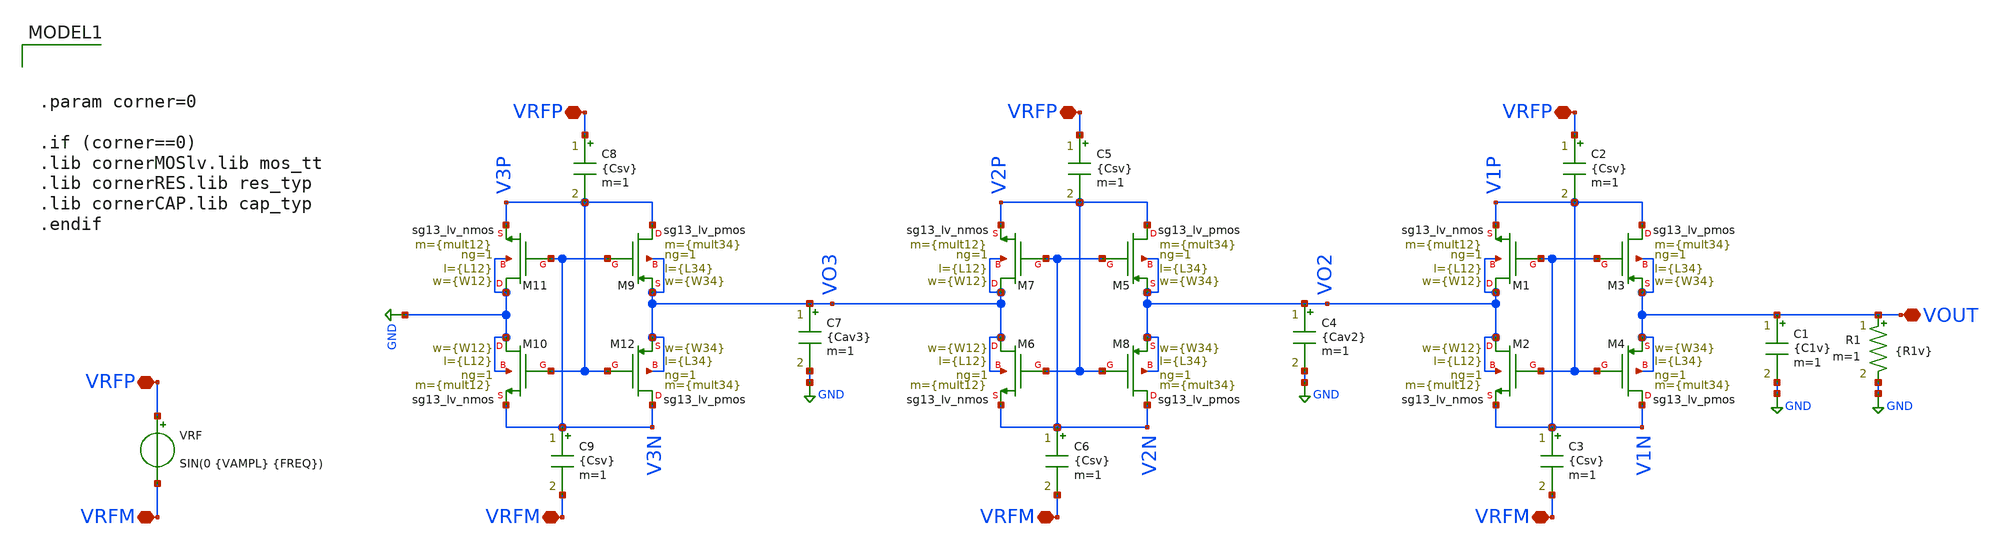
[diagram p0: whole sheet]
** sch_path: Esquematicos_Xschem/Memoria_CCDD_TRAN_MULT3.sch
**.subckt Memoria_CCDD_TRAN_MULT3 VRFP VRFM VOUT VRFP VRFM VRFP VRFM VRFP VRFM
*.iopin VRFP
*.iopin VRFM
*.iopin VOUT
*.iopin VRFP
*.iopin VRFM
*.iopin VRFP
*.iopin VRFM
*.iopin VRFP
*.iopin VRFM
XM3 V1P V1N VOUT VOUT sg13_lv_pmos w={W34} l={L34} ng=1 m={mult34} mm_ok=1
XM2 VO2 V1P V1N VO2 sg13_lv_nmos w={W12} l={L12} ng=1 m={mult12} mm_ok=1
XM1 VO2 V1N V1P VO2 sg13_lv_nmos w={W12} l={L12} ng=1 m={mult12} mm_ok=1
XM4 V1N V1P VOUT VOUT sg13_lv_pmos w={W34} l={L34} ng=1 m={mult34} mm_ok=1
R1 VOUT GND {R1v} m=1
C1 VOUT GND {C1v} m=1
VRF VRFP VRFM SIN(0 {VAMPL} {FREQ})
.save i(vrf)
C2 VRFP V1P {Csv} m=1
C3 V1N VRFM {Csv} m=1
XM5 V2P V2N VO2 VO2 sg13_lv_pmos w={W34} l={L34} ng=1 m={mult34} mm_ok=1
XM6 VO3 V2P V2N VO3 sg13_lv_nmos w={W12} l={L12} ng=1 m={mult12} mm_ok=1
XM7 VO3 V2N V2P VO3 sg13_lv_nmos w={W12} l={L12} ng=1 m={mult12} mm_ok=1
XM8 V2N V2P VO2 VO2 sg13_lv_pmos w={W34} l={L34} ng=1 m={mult34} mm_ok=1
C4 VO2 GND {Cav2} m=1
C5 VRFP V2P {Csv} m=1
C6 V2N VRFM {Csv} m=1
XM9 V3P V3N VO3 VO3 sg13_lv_pmos w={W34} l={L34} ng=1 m={mult34} mm_ok=1
XM10 GND V3P V3N GND sg13_lv_nmos w={W12} l={L12} ng=1 m={mult12} mm_ok=1
XM11 GND V3N V3P GND sg13_lv_nmos w={W12} l={L12} ng=1 m={mult12} mm_ok=1
XM12 V3N V3P VO3 VO3 sg13_lv_pmos w={W34} l={L34} ng=1 m={mult34} mm_ok=1
C7 VO3 GND {Cav3} m=1
C8 VRFP V3P {Csv} m=1
C9 V3N VRFM {Csv} m=1
**** begin user architecture code



.option wnflag=1
.savecurrents

* =============================
* PARAMETROS DE SIMULACION
* =============================

**** Parametros PMOS M3 y M4
.param L34 = 0.2u
.param W34 = 1.78u
.param mult34 = 40

**** Parametros NMOS M1 y M2
.param L12 = 0.2u
.param W12 = 0.6u
.param mult12 = 40

* Parametros PMOS M1
*.param Lval1 = 0.13u
*.param Wval1 = 0.15u
*.param mult1 = 5

* Parametros NMOS M2
*.param Lval2 = 1u
*.param Wval2 = 0.15u
*.param mult2 = 1

* Parametros NMOS M3
*.param Lval3 = 1u
*.param Wval3 = 0.15u
*.param mult3 = 1

* Parametros PMOS M4
*.param Lval4 = 1u
*.param Wval4 = 0.15u
*.param mult4 = 1

**** Parametros de Carga
.param C1v = 1p
.ic V(VOUT) = 0
.param R1v = 5k

**** Parametros de Acople
.param Csv = 4p
.param Cav2 = 2*1p
.param Cav3 = 3*1p
*.param Cav4 = 4*1p
*.param Cav5 = 5*1p

**** Parametros Fuente Sinusoidal
.param VAMPL = 0.1      ; Amplitud (V)
.param VOFFS = 0         ; Valor medio (V)
.param FREQ  = 900MEG        ; Frecuencia (Hz)
.param PHASE = 0         ; Fase1 (grados)








.option wnflag=1
.savecurrents

* ==============================================
* BLOQUE DE CONTROL NGSPICE
* ==============================================
.control

**** Compatibilidad y Color
  set filetype = ascii
  set color0 = white

**** Inicializacion de Parametro While
  let k = 0
  let start_VRF = 0.3
  let stop_VRF = 1.2
  let delta_VRF = 0.1
  let VRF_act = start_VRF

**** Inicializacion Constantes para Calculos
  let i = 0
  let IDmax = 0
  let IGmax = 0
  let VDSmax = 0
  let VGSmax = 0

**** Variables Exteriores


* ==============================================
* Inicio del While
* ==============================================
  while VRF_act le stop_VRF + 2*delta_VRF
    if k = 1
      tran 20p 500n UIC
    end
    alterparam VAMPL = $&VRF_act
    reset

* -----------------------------
* Almacenamiento de Variables
* -----------------------------
    save all

    **** M2
    save @n.xm2.nsg13_lv_nmos[ids]
    save @n.xm2.nsg13_lv_nmos[igs]
    save @n.xm2.nsg13_lv_nmos[gm]
    save @n.xm2.nsg13_lv_nmos[gds]
    save @n.xm2.nsg13_lv_nmos[vth]

    **** M6
    save @n.xm6.nsg13_lv_nmos[ids]
    save @n.xm6.nsg13_lv_nmos[igs]
    save @n.xm6.nsg13_lv_nmos[gm]
    save @n.xm6.nsg13_lv_nmos[gds]
    save @n.xm6.nsg13_lv_nmos[vth]

    **** M10
    save @n.xm10.nsg13_lv_nmos[ids]
    save @n.xm10.nsg13_lv_nmos[igs]
    save @n.xm10.nsg13_lv_nmos[gm]
    save @n.xm10.nsg13_lv_nmos[gds]
    save @n.xm10.nsg13_lv_nmos[vth]

    **** Fuente de Voltaje
    save @VRF[i]
    save @VRF[p]

    **** Carga
    save R1[i]
    save C1[i]

* ----------------------------------------------
* Definicion de Varriables Internas
* ----------------------------------------------
    if k = 1

      **** M2
      let ids2 = @n.xm2.nsg13_lv_nmos[ids]
      let igs2 = @n.xm2.nsg13_lv_nmos[igs]
      let gm2 = @n.xm2.nsg13_lv_nmos[gm]
      let gds2 =  @n.xm2.nsg13_lv_nmos[gds]
      let vth2 = @n.xm2.nsg13_lv_nmos[vth]
      let VDS2 = V1N - VO2
      let VGS2 = V1P - VO2

      **** M6
      let ids6 = @n.xm6.nsg13_lv_nmos[ids]
      let igs6 = @n.xm6.nsg13_lv_nmos[igs]
      let gm6 = @n.xm6.nsg13_lv_nmos[gm]
      let gds6 =  @n.xm6.nsg13_lv_nmos[gds]
      let vth6 = @n.xm6.nsg13_lv_nmos[vth]
      let VDS6 = V2N - VO3
      let VGS6 = V2P - VO3

      **** M10
      let ids10 = @n.xm10.nsg13_lv_nmos[ids]
      let igs10 = @n.xm10.nsg13_lv_nmos[igs]
      let gm10 = @n.xm10.nsg13_lv_nmos[gm]
      let gds10 =  @n.xm10.nsg13_lv_nmos[gds]
      let vth10 = @n.xm10.nsg13_lv_nmos[vth]
      let VDS10 = V3N - 0
      let VGS10 = V3P - 0

      **** Fuente de Voltaje
      let IRF = @VRF[i]
      let PRF = @VRF[p]
      let VRF = VRFP - VRFM

      **** Carga
      let IC = @C1[i]
      let IR = @R1[i]
      let IRC = IC + IR
      let PR = IR * VOUT

    end


* ==============================================
* RESULTADOS
* ==============================================

* -----------------------------
* Graficas de la Simulacion
* -----------------------------
    if k = 1
    **** Fuente
    *plot VRF vs time
    *plot IRF vs time

    **** Carga
    plot VOUT VRF vs time
    *plot IRC vs time
    *plot avg(PR/PRF)
    end

* -----------------------------
* Registro de Datos
* -----------------------------
    remzerovec
    write Memoria_CCDD2_TRAN_MULT3_L00-20_W00-60_R005k_M40_C04-00.csv time VRF IRF VOUT VO2 VO3 IC
+ IR VDS2 VDS6 VDS10 VGS2 VGS6 VGS10 ids2 ids6 ids10 igs2 igs6 igs10


* ==============================================
* CIERRE DE WHILE
* ==============================================
    **** Definicion de proximo valor (while)
    let VRF_act = VRF_act + delta_VRF
    let k = 1
    set appendwrite

  end

.endc




.param corner=0

.if (corner==0)
.lib cornerMOSlv.lib mos_tt
.lib cornerRES.lib res_typ
.lib cornerCAP.lib cap_typ
.endif

**** end user architecture code
**.ends
.GLOBAL GND
.end
